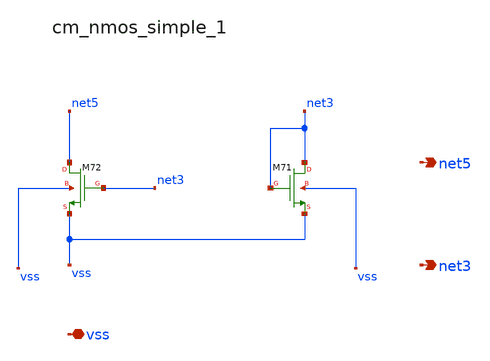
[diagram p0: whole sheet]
** sch_path: analog-db/raw/amp_017_tan_clia/hier/blocks/cm_nmos_simple_1.sch
**.subckt cm_nmos_simple_1 vss net5 net3
*.iopin vss
*.opin net5
*.opin net3
XM71 net3 net3 vss vss sg13_lv_nmos w=x_dut_xm71_w l=x_dut_xm71_l ng=1 m=x_dut_xm71_m
XM72 net5 net3 vss vss sg13_lv_nmos w=x_dut_xm72_w l=x_dut_xm72_l ng=1 m=x_dut_xm72_m
**.ends
.end
